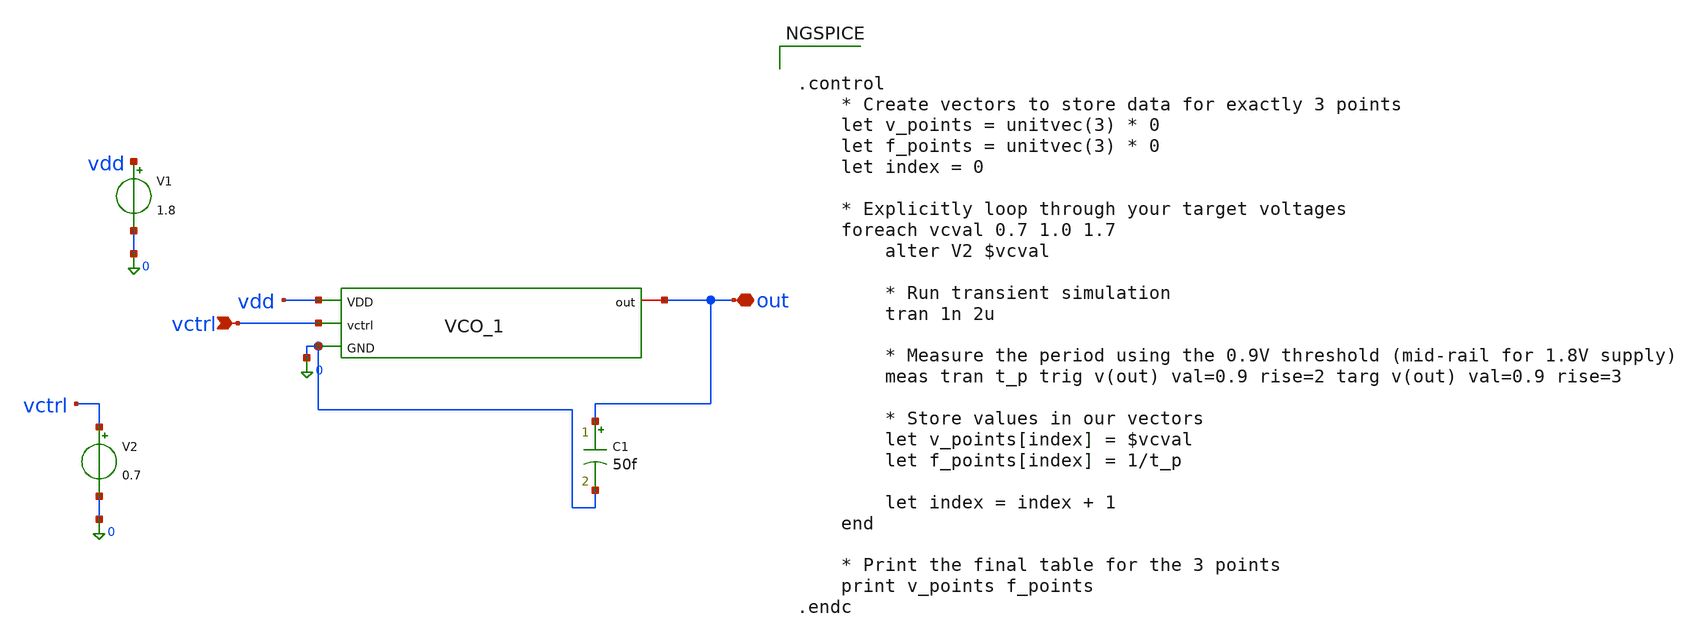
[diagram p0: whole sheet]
** sch_path: design_data/xschem/VCO/vco_tb_op.sch
**.subckt vco_tb_op vctrl out
*.ipin vctrl
*.iopin out
V1 vdd 0 1.8
V2 vctrl 0 0.7
C1 out 0 50f m=1
x1 vdd out vctrl 0 vco_1
**** begin user architecture code


.control
    * Create vectors to store data for exactly 3 points
    let v_points = unitvec(3) * 0
    let f_points = unitvec(3) * 0
    let index = 0

    * Explicitly loop through your target voltages
    foreach vcval 0.7 1.0 1.7
        alter V2 $vcval

        * Run transient simulation
        tran 1n 2u

        * Measure the period using the 0.9V threshold (mid-rail for 1.8V supply)
        meas tran t_p trig v(out) val=0.9 rise=2 targ v(out) val=0.9 rise=3

        * Store values in our vectors
        let v_points[index] = $vcval
        let f_points[index] = 1/t_p

        let index = index + 1
    end

    * Print the final table for the 3 points
    print v_points f_points
.endc



** opencircuitdesign pdks install
.lib $::SKYWATER_MODELS/sky130.lib.spice tt

**** end user architecture code
**.ends

* expanding   symbol:  xschem/VCO/vco_1.sym # of pins=4
** sym_path: design_data/xschem/VCO/vco_1.sym
** sch_path: design_data/xschem/VCO/vco_1.sch
.subckt vco_1 VDD out vctrl GND
*.ipin vctrl
*.iopin out
*.ipin GND
*.ipin VDD
XM7 net4 net4 VDD VDD sky130_fd_pr__pfet_01v8 L=3.2 W=70 nf=1 ad='int((1 + 1)/2) * 70 / 1 * 0.29' as='int((1 + 2)/2) * 70 / 1 * 0.29'
+ pd='2*int((1 + 1)/2) * (70 / 1 + 0.29)' ps='2*int((1 + 2)/2) * (70 / 1 + 0.29)' nrd='0.29 / 70 ' nrs='0.29 / 70 '
+ sa=0 sb=0 sd=0 mult=1 m=1
XM8 net4 vctrl GND GND sky130_fd_pr__nfet_01v8 L=4.2 W=40 nf=1 ad='int((1 + 1)/2) * 40 / 1 * 0.29' as='int((1 + 2)/2) * 40 / 1 * 0.29'
+ pd='2*int((1 + 1)/2) * (40 / 1 + 0.29)' ps='2*int((1 + 2)/2) * (40 / 1 + 0.29)' nrd='0.29 / 40 ' nrs='0.29 / 40 '
+ sa=0 sb=0 sd=0 mult=1 m=1
XM5 net11 vctrl GND GND sky130_fd_pr__nfet_01v8 L=4.2 W=40 nf=1 ad='int((1 + 1)/2) * 40 / 1 * 0.29' as='int((1 + 2)/2) * 40 / 1 * 0.29'
+ pd='2*int((1 + 1)/2) * (40 / 1 + 0.29)' ps='2*int((1 + 2)/2) * (40 / 1 + 0.29)' nrd='0.29 / 40 ' nrs='0.29 / 40 '
+ sa=0 sb=0 sd=0 mult=1 m=1
XM6 net1 net3 net11 GND sky130_fd_pr__nfet_01v8 L=1.4 W=49 nf=1 ad='int((1 + 1)/2) * 49 / 1 * 0.29' as='int((1 + 2)/2) * 49 / 1 * 0.29'
+ pd='2*int((1 + 1)/2) * (49 / 1 + 0.29)' ps='2*int((1 + 2)/2) * (49 / 1 + 0.29)' nrd='0.29 / 49 ' nrs='0.29 / 49 '
+ sa=0 sb=0 sd=0 mult=1 m=1
XM1 net2 net4 VDD VDD sky130_fd_pr__pfet_01v8 L=3.2 W=70 nf=1 ad='int((1 + 1)/2) * 70 / 1 * 0.29' as='int((1 + 2)/2) * 70 / 1 * 0.29'
+ pd='2*int((1 + 1)/2) * (70 / 1 + 0.29)' ps='2*int((1 + 2)/2) * (70 / 1 + 0.29)' nrd='0.29 / 70 ' nrs='0.29 / 70 '
+ sa=0 sb=0 sd=0 mult=1 m=1
XM2 net1 net3 net2 net2 sky130_fd_pr__pfet_01v8 L=1.4 W=74 nf=1 ad='int((1 + 1)/2) * 74 / 1 * 0.29' as='int((1 + 2)/2) * 74 / 1 * 0.29'
+ pd='2*int((1 + 1)/2) * (74 / 1 + 0.29)' ps='2*int((1 + 2)/2) * (74 / 1 + 0.29)' nrd='0.29 / 74 ' nrs='0.29 / 74 '
+ sa=0 sb=0 sd=0 mult=1 m=1
XM3 net10 vctrl GND GND sky130_fd_pr__nfet_01v8 L=4.2 W=40 nf=1 ad='int((1 + 1)/2) * 40 / 1 * 0.29' as='int((1 + 2)/2) * 40 / 1 * 0.29'
+ pd='2*int((1 + 1)/2) * (40 / 1 + 0.29)' ps='2*int((1 + 2)/2) * (40 / 1 + 0.29)' nrd='0.29 / 40 ' nrs='0.29 / 40 '
+ sa=0 sb=0 sd=0 mult=1 m=1
XM9 net5 net4 VDD VDD sky130_fd_pr__pfet_01v8 L=3.2 W=70 nf=1 ad='int((1 + 1)/2) * 70 / 1 * 0.29' as='int((1 + 2)/2) * 70 / 1 * 0.29'
+ pd='2*int((1 + 1)/2) * (70 / 1 + 0.29)' ps='2*int((1 + 2)/2) * (70 / 1 + 0.29)' nrd='0.29 / 70 ' nrs='0.29 / 70 '
+ sa=0 sb=0 sd=0 mult=1 m=1
XM11 net9 vctrl GND GND sky130_fd_pr__nfet_01v8 L=4.2 W=40 nf=1 ad='int((1 + 1)/2) * 40 / 1 * 0.29' as='int((1 + 2)/2) * 40 / 1 * 0.29'
+ pd='2*int((1 + 1)/2) * (40 / 1 + 0.29)' ps='2*int((1 + 2)/2) * (40 / 1 + 0.29)' nrd='0.29 / 40 ' nrs='0.29 / 40 '
+ sa=0 sb=0 sd=0 mult=1 m=1
XM13 net6 net4 VDD VDD sky130_fd_pr__pfet_01v8 L=3.2 W=70 nf=1 ad='int((1 + 1)/2) * 70 / 1 * 0.29' as='int((1 + 2)/2) * 70 / 1 * 0.29'
+ pd='2*int((1 + 1)/2) * (70 / 1 + 0.29)' ps='2*int((1 + 2)/2) * (70 / 1 + 0.29)' nrd='0.29 / 70 ' nrs='0.29 / 70 '
+ sa=0 sb=0 sd=0 mult=1 m=1
XM4 net7 net1 net10 GND sky130_fd_pr__nfet_01v8 L=1.4 W=49 nf=1 ad='int((1 + 1)/2) * 49 / 1 * 0.29' as='int((1 + 2)/2) * 49 / 1 * 0.29'
+ pd='2*int((1 + 1)/2) * (49 / 1 + 0.29)' ps='2*int((1 + 2)/2) * (49 / 1 + 0.29)' nrd='0.29 / 49 ' nrs='0.29 / 49 '
+ sa=0 sb=0 sd=0 mult=1 m=1
XM10 net7 net1 net5 net5 sky130_fd_pr__pfet_01v8 L=1.4 W=74 nf=1 ad='int((1 + 1)/2) * 74 / 1 * 0.29'
+ as='int((1 + 2)/2) * 74 / 1 * 0.29' pd='2*int((1 + 1)/2) * (74 / 1 + 0.29)' ps='2*int((1 + 2)/2) * (74 / 1 + 0.29)'
+ nrd='0.29 / 74 ' nrs='0.29 / 74 ' sa=0 sb=0 sd=0 mult=1 m=1
XM12 net3 net7 net9 GND sky130_fd_pr__nfet_01v8 L=1.4 W=49 nf=1 ad='int((1 + 1)/2) * 49 / 1 * 0.29' as='int((1 + 2)/2) * 49 / 1 * 0.29'
+ pd='2*int((1 + 1)/2) * (49 / 1 + 0.29)' ps='2*int((1 + 2)/2) * (49 / 1 + 0.29)' nrd='0.29 / 49 ' nrs='0.29 / 49 '
+ sa=0 sb=0 sd=0 mult=1 m=1
XM14 net3 net7 net6 net6 sky130_fd_pr__pfet_01v8 L=1.4 W=74 nf=1 ad='int((1 + 1)/2) * 74 / 1 * 0.29'
+ as='int((1 + 2)/2) * 74 / 1 * 0.29' pd='2*int((1 + 1)/2) * (74 / 1 + 0.29)' ps='2*int((1 + 2)/2) * (74 / 1 + 0.29)'
+ nrd='0.29 / 74 ' nrs='0.29 / 74 ' sa=0 sb=0 sd=0 mult=1 m=1
XM15 net8 net3 GND GND sky130_fd_pr__nfet_01v8 L=1 W=10 nf=1 ad='int((1 + 1)/2) * 10 / 1 * 0.29' as='int((1 + 2)/2) * 10 / 1 * 0.29'
+ pd='2*int((1 + 1)/2) * (10 / 1 + 0.29)' ps='2*int((1 + 2)/2) * (10 / 1 + 0.29)' nrd='0.29 / 10 ' nrs='0.29 / 10 '
+ sa=0 sb=0 sd=0 mult=1 m=1
XM16 net8 net3 VDD VDD sky130_fd_pr__pfet_01v8 L=1 W=20 nf=1 ad='int((1 + 1)/2) * 20 / 1 * 0.29' as='int((1 + 2)/2) * 20 / 1 * 0.29'
+ pd='2*int((1 + 1)/2) * (20 / 1 + 0.29)' ps='2*int((1 + 2)/2) * (20 / 1 + 0.29)' nrd='0.29 / 20 ' nrs='0.29 / 20 '
+ sa=0 sb=0 sd=0 mult=1 m=1
XM17 out net8 GND GND sky130_fd_pr__nfet_01v8 L=1 W=20 nf=1 ad='int((1 + 1)/2) * 20 / 1 * 0.29' as='int((1 + 2)/2) * 20 / 1 * 0.29'
+ pd='2*int((1 + 1)/2) * (20 / 1 + 0.29)' ps='2*int((1 + 2)/2) * (20 / 1 + 0.29)' nrd='0.29 / 20 ' nrs='0.29 / 20 '
+ sa=0 sb=0 sd=0 mult=1 m=1
XM18 out net8 VDD VDD sky130_fd_pr__pfet_01v8 L=1 W=40 nf=1 ad='int((1 + 1)/2) * 40 / 1 * 0.29' as='int((1 + 2)/2) * 40 / 1 * 0.29'
+ pd='2*int((1 + 1)/2) * (40 / 1 + 0.29)' ps='2*int((1 + 2)/2) * (40 / 1 + 0.29)' nrd='0.29 / 40 ' nrs='0.29 / 40 '
+ sa=0 sb=0 sd=0 mult=1 m=1
.ends

.end
